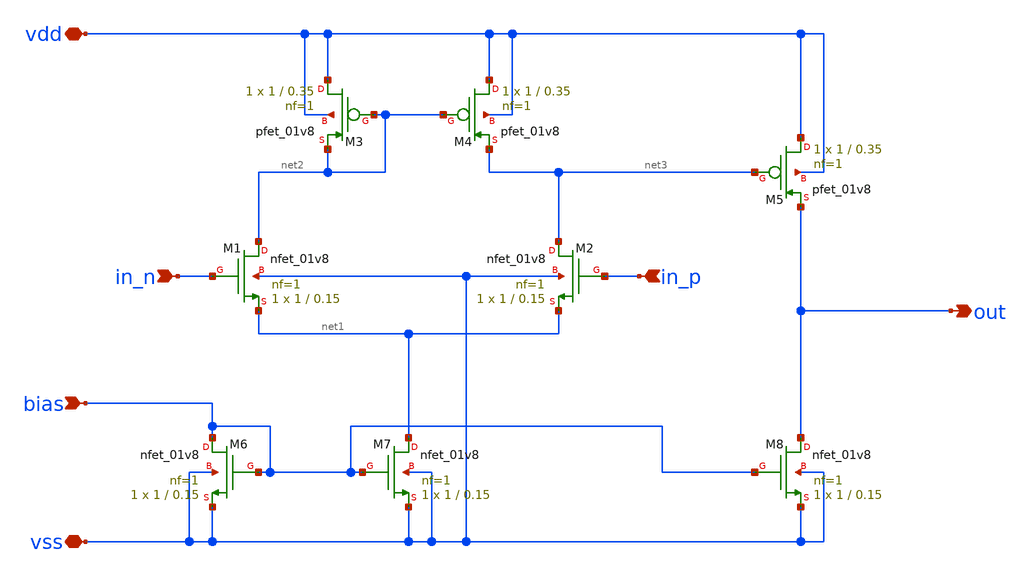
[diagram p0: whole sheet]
** sch_path: design/myopamp/myopamp.sch
**.subckt myopamp in_n in_p bias out vdd vss
*.ipin in_n
*.ipin in_p
*.ipin bias
*.opin out
*.iopin vdd
*.iopin vss
XM1 net2 in_n net1 vss sky130_fd_pr__nfet_01v8 L=0.15 W=1 nf=1 ad='int((nf+1)/2) * W/nf * 0.29' as='int((nf+2)/2) * W/nf * 0.29'
+ pd='2*int((nf+1)/2) * (W/nf + 0.29)' ps='2*int((nf+2)/2) * (W/nf + 0.29)' nrd='0.29 / W' nrs='0.29 / W'
+ sa=0 sb=0 sd=0 mult=1 m=1
XM2 net3 in_p net1 vss sky130_fd_pr__nfet_01v8 L=0.15 W=1 nf=1 ad='int((nf+1)/2) * W/nf * 0.29' as='int((nf+2)/2) * W/nf * 0.29'
+ pd='2*int((nf+1)/2) * (W/nf + 0.29)' ps='2*int((nf+2)/2) * (W/nf + 0.29)' nrd='0.29 / W' nrs='0.29 / W'
+ sa=0 sb=0 sd=0 mult=1 m=1
XM3 vdd net2 net2 vdd sky130_fd_pr__pfet_01v8 L=0.35 W=1 nf=1 ad='int((nf+1)/2) * W/nf * 0.29' as='int((nf+2)/2) * W/nf * 0.29'
+ pd='2*int((nf+1)/2) * (W/nf + 0.29)' ps='2*int((nf+2)/2) * (W/nf + 0.29)' nrd='0.29 / W' nrs='0.29 / W'
+ sa=0 sb=0 sd=0 mult=1 m=1
XM4 vdd net2 net3 vdd sky130_fd_pr__pfet_01v8 L=0.35 W=1 nf=1 ad='int((nf+1)/2) * W/nf * 0.29' as='int((nf+2)/2) * W/nf * 0.29'
+ pd='2*int((nf+1)/2) * (W/nf + 0.29)' ps='2*int((nf+2)/2) * (W/nf + 0.29)' nrd='0.29 / W' nrs='0.29 / W'
+ sa=0 sb=0 sd=0 mult=1 m=1
XM5 vdd net3 out vdd sky130_fd_pr__pfet_01v8 L=0.35 W=1 nf=1 ad='int((nf+1)/2) * W/nf * 0.29' as='int((nf+2)/2) * W/nf * 0.29'
+ pd='2*int((nf+1)/2) * (W/nf + 0.29)' ps='2*int((nf+2)/2) * (W/nf + 0.29)' nrd='0.29 / W' nrs='0.29 / W'
+ sa=0 sb=0 sd=0 mult=1 m=1
XM6 bias bias vss vss sky130_fd_pr__nfet_01v8 L=0.15 W=1 nf=1 ad='int((nf+1)/2) * W/nf * 0.29' as='int((nf+2)/2) * W/nf * 0.29'
+ pd='2*int((nf+1)/2) * (W/nf + 0.29)' ps='2*int((nf+2)/2) * (W/nf + 0.29)' nrd='0.29 / W' nrs='0.29 / W'
+ sa=0 sb=0 sd=0 mult=1 m=1
XM7 net1 bias vss vss sky130_fd_pr__nfet_01v8 L=0.15 W=1 nf=1 ad='int((nf+1)/2) * W/nf * 0.29' as='int((nf+2)/2) * W/nf * 0.29'
+ pd='2*int((nf+1)/2) * (W/nf + 0.29)' ps='2*int((nf+2)/2) * (W/nf + 0.29)' nrd='0.29 / W' nrs='0.29 / W'
+ sa=0 sb=0 sd=0 mult=1 m=1
XM8 out bias vss vss sky130_fd_pr__nfet_01v8 L=0.15 W=1 nf=1 ad='int((nf+1)/2) * W/nf * 0.29' as='int((nf+2)/2) * W/nf * 0.29'
+ pd='2*int((nf+1)/2) * (W/nf + 0.29)' ps='2*int((nf+2)/2) * (W/nf + 0.29)' nrd='0.29 / W' nrs='0.29 / W'
+ sa=0 sb=0 sd=0 mult=1 m=1
**.ends
.end
